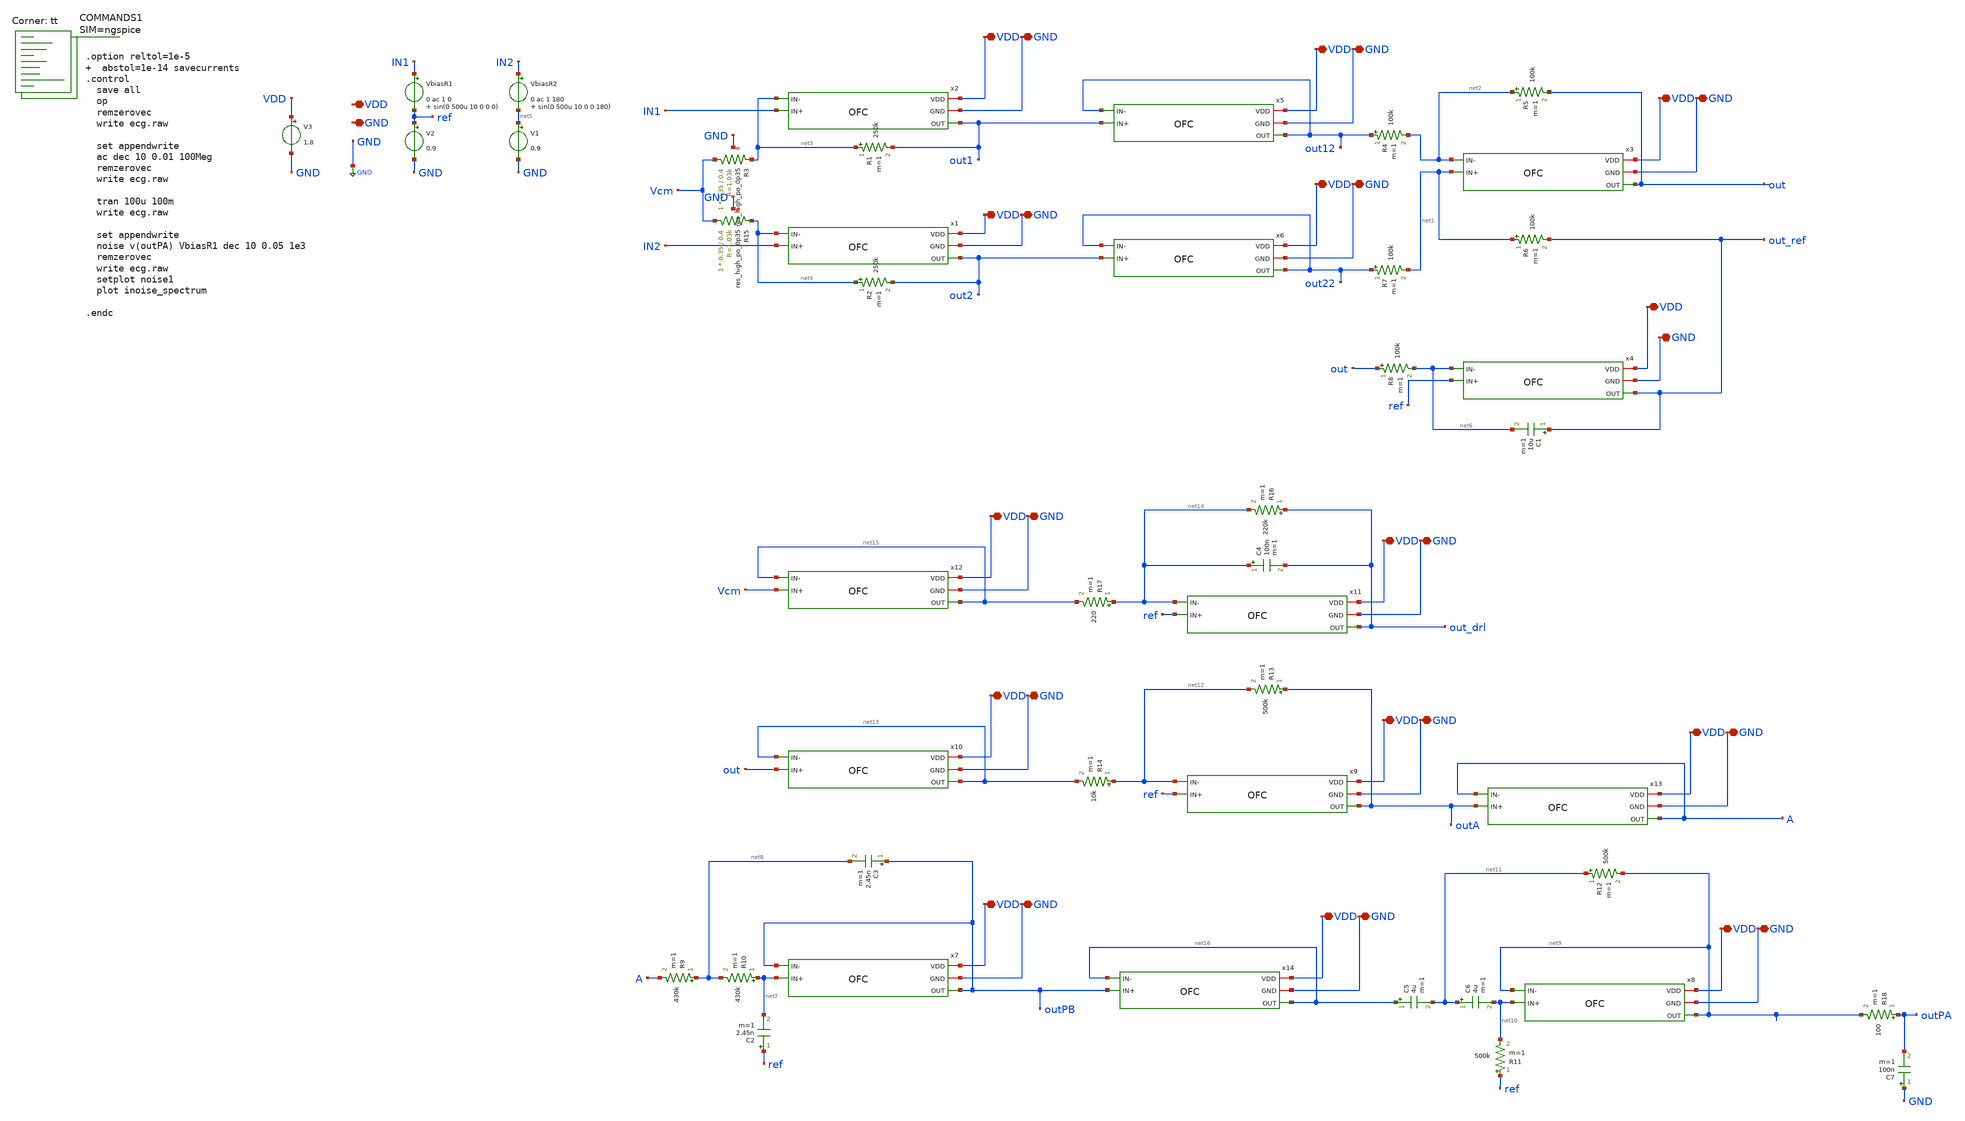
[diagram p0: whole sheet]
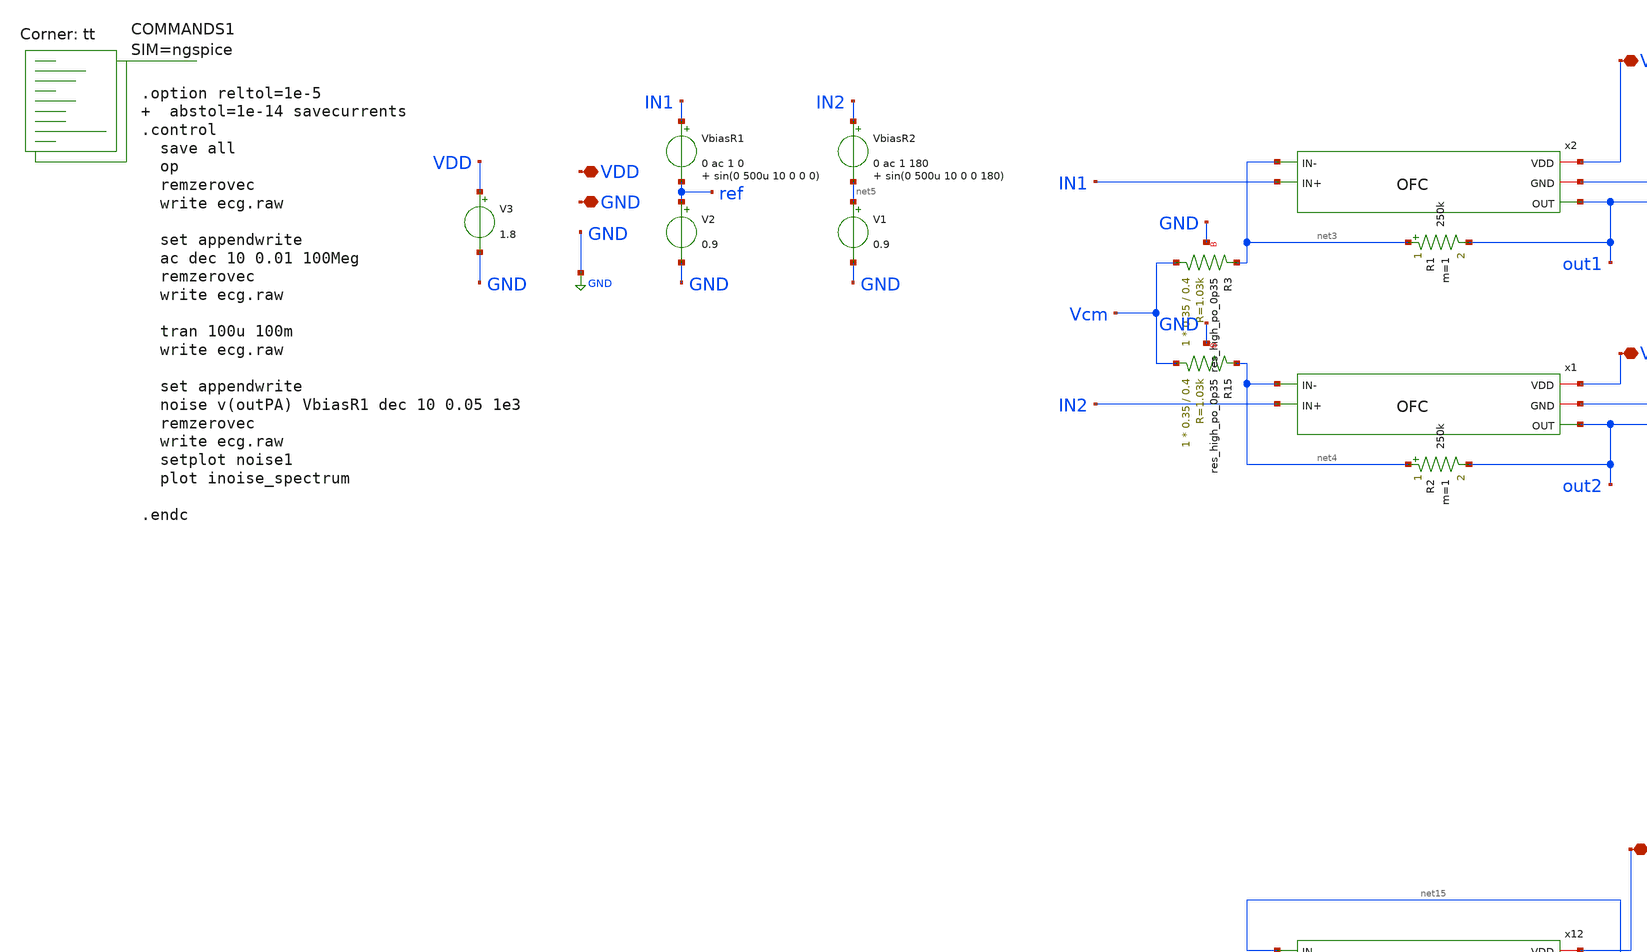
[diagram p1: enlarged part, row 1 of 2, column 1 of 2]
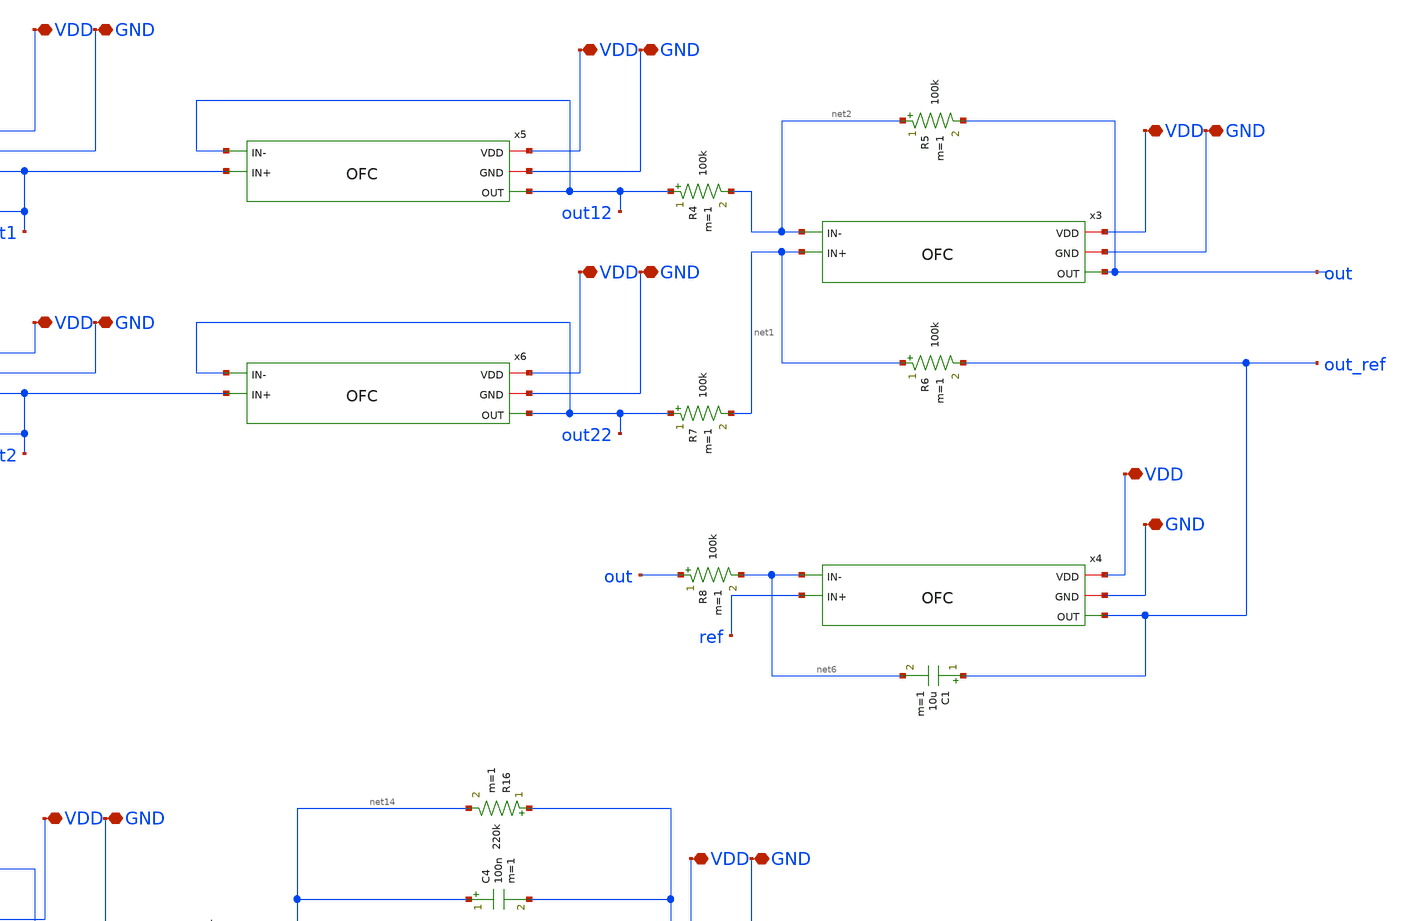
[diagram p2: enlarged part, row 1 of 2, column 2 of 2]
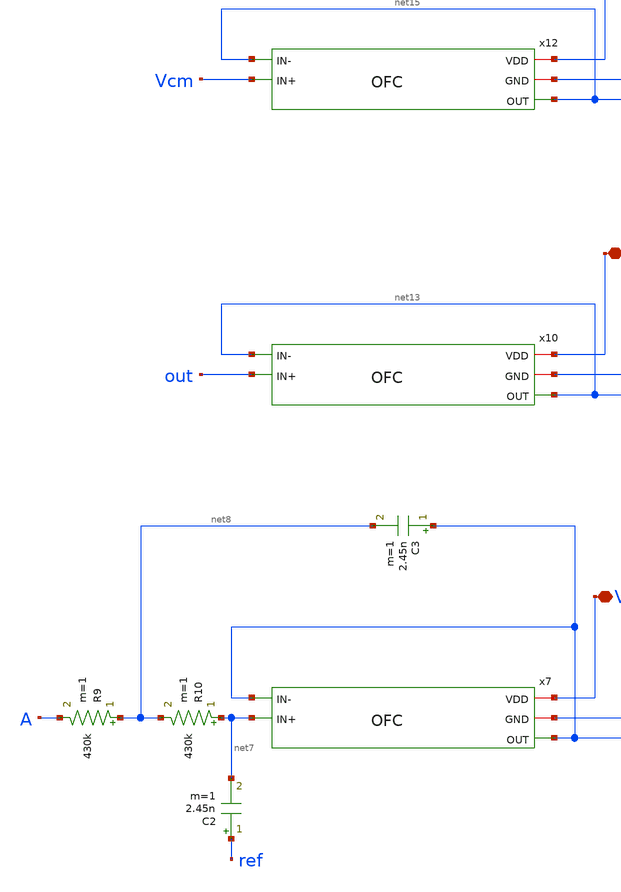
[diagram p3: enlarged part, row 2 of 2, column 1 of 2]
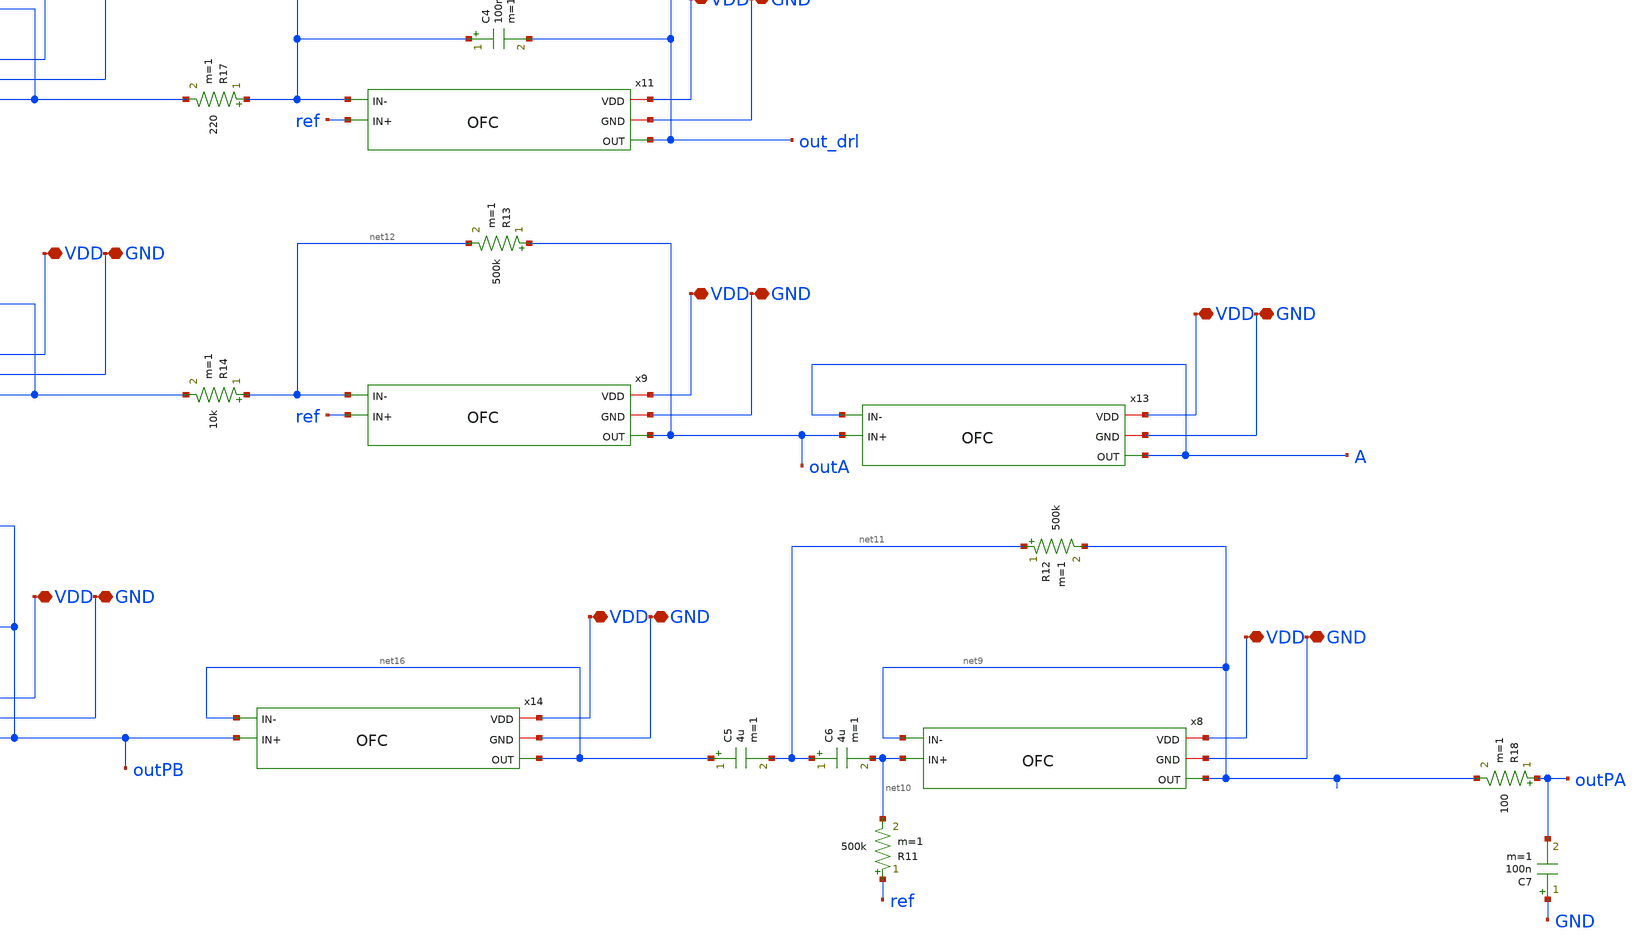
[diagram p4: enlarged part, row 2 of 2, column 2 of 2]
** sch_path: xschem/untitled-6.sch
**.subckt untitled-6 VDD GND VDD VDD GND GND VDD GND VDD GND VDD GND VDD GND VDD GND VDD GND VDD GND
*+ VDD GND VDD GND VDD GND VDD GND VDD GND
*.iopin VDD
*.iopin GND
*.iopin VDD
*.iopin VDD
*.iopin GND
*.iopin GND
*.iopin VDD
*.iopin GND
*.iopin VDD
*.iopin GND
*.iopin VDD
*.iopin GND
*.iopin VDD
*.iopin GND
*.iopin VDD
*.iopin GND
*.iopin VDD
*.iopin GND
*.iopin VDD
*.iopin GND
*.iopin VDD
*.iopin GND
*.iopin VDD
*.iopin GND
*.iopin VDD
*.iopin GND
*.iopin VDD
*.iopin GND
*.iopin VDD
*.iopin GND
x1 VDD GND out2 net4 IN2 OFC
x2 VDD GND out1 net3 IN1 OFC
x3 VDD GND out net2 net1 OFC
V3 VDD GND 1.8
VbiasR1 IN1 ref 0 ac 1 0 sin(0 500u 10 0 0 0)
V2 ref GND 0.9
VbiasR2 IN2 net5 0 ac 1 180 sin(0 500u 10 0 0 180)
V1 net5 GND 0.9
R1 net3 out1 250k m=1
R2 net4 out2 250k m=1
x4 VDD GND out_ref net6 ref OFC
R6 net1 out_ref 100k m=1
R8 out net6 100k m=1
C1 out_ref net6 10u m=1
R5 net2 out 100k m=1
x5 VDD GND out12 out12 out1 OFC
x6 VDD GND out22 out22 out2 OFC
R4 out12 net2 100k m=1
R7 out22 net1 100k m=1
x7 VDD GND outPB outPB net7 OFC
R9 net8 A 430k m=1
C2 ref net7 2.45n m=1
R10 net7 net8 430k m=1
C3 outPB net8 2.45n m=1
x8 VDD GND net9 net9 net10 OFC
R11 ref net10 500k m=1
C5 net16 net11 4u m=1
C6 net11 net10 4u m=1
x9 VDD GND outA net12 ref OFC
R13 outA net12 500k m=1
R14 net12 net13 10k m=1
x10 VDD GND net13 net13 out OFC
x11 VDD GND out_drl net14 ref OFC
R16 out_drl net14 220k m=1
R17 net14 net15 220 m=1
x12 VDD GND net15 net15 Vcm OFC
C4 net14 out_drl 100n m=1
x13 VDD GND A A outA OFC
x14 VDD GND net16 net16 outPB OFC
C7 GND outPA 100n m=1
R18 outPA net9 100 m=1
R12 net11 net9 500k m=1
XR3 Vcm net3 GND sky130_fd_pr__res_high_po_0p35 L=0.4 mult=1 m=1
XR15 Vcm net4 GND sky130_fd_pr__res_high_po_0p35 L=0.4 mult=1 m=1
**** begin user architecture code



.option reltol=1e-5   abstol=1e-14 savecurrents
.control
  save all
  op
  remzerovec
  write ecg.raw

  set appendwrite
  ac dec 10 0.01 100Meg
  remzerovec
  write ecg.raw

  tran 100u 100m
  write ecg.raw

  set appendwrite
  noise v(outPA) VbiasR1 dec 10 0.05 1e3
  remzerovec
  write ecg.raw
  setplot noise1
  plot inoise_spectrum

.endc



.lib $::SKYWATER_MODELS/sky130.lib.spice tt
**** end user architecture code
**.ends

* expanding   symbol:  OFC.sym # of pins=5
** sym_path: OFC.sym
** sch_path: OFC.sch
.subckt OFC VDD GND OUT IN- IN+
*.iopin VDD
*.iopin GND
*.ipin IN+
*.ipin IN-
*.opin OUT
XM11 S Vb VDD VDD sky130_fd_pr__pfet_01v8_lvt L=1 W=60 nf=2 ad='int((nf+1)/2) * W/nf * 0.29' as='int((nf+2)/2) * W/nf * 0.29'
+ pd='2*int((nf+1)/2) * (W/nf + 0.29)' ps='2*int((nf+2)/2) * (W/nf + 0.29)' nrd='0.29 / W' nrs='0.29 / W'
+ sa=0 sb=0 sd=0 mult=2 m=2
XM1 D1 IN+ S S sky130_fd_pr__pfet_01v8_lvt L=10 W=25 nf=2 ad='int((nf+1)/2) * W/nf * 0.29' as='int((nf+2)/2) * W/nf * 0.29'
+ pd='2*int((nf+1)/2) * (W/nf + 0.29)' ps='2*int((nf+2)/2) * (W/nf + 0.29)' nrd='0.29 / W' nrs='0.29 / W'
+ sa=0 sb=0 sd=0 mult=2 m=2
XM2 D2 IN- S S sky130_fd_pr__pfet_01v8_lvt L=10 W=25 nf=2 ad='int((nf+1)/2) * W/nf * 0.29' as='int((nf+2)/2) * W/nf * 0.29'
+ pd='2*int((nf+1)/2) * (W/nf + 0.29)' ps='2*int((nf+2)/2) * (W/nf + 0.29)' nrd='0.29 / W' nrs='0.29 / W'
+ sa=0 sb=0 sd=0 mult=2 m=2
XM3 OUT Vc1 D2 GND sky130_fd_pr__nfet_01v8_lvt L=1 W=4 nf=1 ad='int((nf+1)/2) * W/nf * 0.29' as='int((nf+2)/2) * W/nf * 0.29'
+ pd='2*int((nf+1)/2) * (W/nf + 0.29)' ps='2*int((nf+2)/2) * (W/nf + 0.29)' nrd='0.29 / W' nrs='0.29 / W'
+ sa=0 sb=0 sd=0 mult=1 m=1
XM4 D2 Vc GND GND sky130_fd_pr__nfet_01v8_lvt L=1 W=2.8 nf=1 ad='int((nf+1)/2) * W/nf * 0.29' as='int((nf+2)/2) * W/nf * 0.29'
+ pd='2*int((nf+1)/2) * (W/nf + 0.29)' ps='2*int((nf+2)/2) * (W/nf + 0.29)' nrd='0.29 / W' nrs='0.29 / W'
+ sa=0 sb=0 sd=0 mult=1 m=1
XM5 D1 Vc GND GND sky130_fd_pr__nfet_01v8_lvt L=1 W=2.8 nf=1 ad='int((nf+1)/2) * W/nf * 0.29' as='int((nf+2)/2) * W/nf * 0.29'
+ pd='2*int((nf+1)/2) * (W/nf + 0.29)' ps='2*int((nf+2)/2) * (W/nf + 0.29)' nrd='0.29 / W' nrs='0.29 / W'
+ sa=0 sb=0 sd=0 mult=1 m=1
XM6 G Vc1 D1 GND sky130_fd_pr__nfet_01v8_lvt L=1 W=4 nf=1 ad='int((nf+1)/2) * W/nf * 0.29' as='int((nf+2)/2) * W/nf * 0.29'
+ pd='2*int((nf+1)/2) * (W/nf + 0.29)' ps='2*int((nf+2)/2) * (W/nf + 0.29)' nrd='0.29 / W' nrs='0.29 / W'
+ sa=0 sb=0 sd=0 mult=1 m=1
XM7 G Vc2 D9 D9 sky130_fd_pr__pfet_01v8_lvt L=2.23 W=3 nf=1 ad='int((nf+1)/2) * W/nf * 0.29' as='int((nf+2)/2) * W/nf * 0.29'
+ pd='2*int((nf+1)/2) * (W/nf + 0.29)' ps='2*int((nf+2)/2) * (W/nf + 0.29)' nrd='0.29 / W' nrs='0.29 / W'
+ sa=0 sb=0 sd=0 mult=1 m=1
XM9 D9 G VDD VDD sky130_fd_pr__pfet_01v8_lvt L=2.23 W=4 nf=1 ad='int((nf+1)/2) * W/nf * 0.29' as='int((nf+2)/2) * W/nf * 0.29'
+ pd='2*int((nf+1)/2) * (W/nf + 0.29)' ps='2*int((nf+2)/2) * (W/nf + 0.29)' nrd='0.29 / W' nrs='0.29 / W'
+ sa=0 sb=0 sd=0 mult=1 m=1
XM8 D10 G VDD VDD sky130_fd_pr__pfet_01v8_lvt L=2.23 W=4 nf=1 ad='int((nf+1)/2) * W/nf * 0.29' as='int((nf+2)/2) * W/nf * 0.29'
+ pd='2*int((nf+1)/2) * (W/nf + 0.29)' ps='2*int((nf+2)/2) * (W/nf + 0.29)' nrd='0.29 / W' nrs='0.29 / W'
+ sa=0 sb=0 sd=0 mult=1 m=1
XM10 OUT Vc2 D10 D10 sky130_fd_pr__pfet_01v8_lvt L=2.23 W=3 nf=1 ad='int((nf+1)/2) * W/nf * 0.29' as='int((nf+2)/2) * W/nf * 0.29'
+ pd='2*int((nf+1)/2) * (W/nf + 0.29)' ps='2*int((nf+2)/2) * (W/nf + 0.29)' nrd='0.29 / W' nrs='0.29 / W'
+ sa=0 sb=0 sd=0 mult=1 m=1
XR2 Vb VDD GND sky130_fd_pr__res_xhigh_po_0p35 L=5 mult=1 m=1
XR3 GND Vb GND sky130_fd_pr__res_xhigh_po_0p35 L=13.2 mult=1 m=1
XR1 Vc VDD GND sky130_fd_pr__res_xhigh_po_0p35 L=5 mult=1 m=1
XR4 GND Vc GND sky130_fd_pr__res_xhigh_po_0p35 L=3.07 mult=1 m=1
XR5 Vc1 VDD GND sky130_fd_pr__res_xhigh_po_0p35 L=5 mult=1 m=1
XR6 GND Vc1 GND sky130_fd_pr__res_xhigh_po_0p35 L=13.2 mult=1 m=1
XR7 Vc2 VDD GND sky130_fd_pr__res_xhigh_po_0p35 L=5 mult=1 m=1
XR8 GND Vc2 GND sky130_fd_pr__res_xhigh_po_0p35 L=1.6 mult=1 m=1
.ends

.GLOBAL GND
.end
